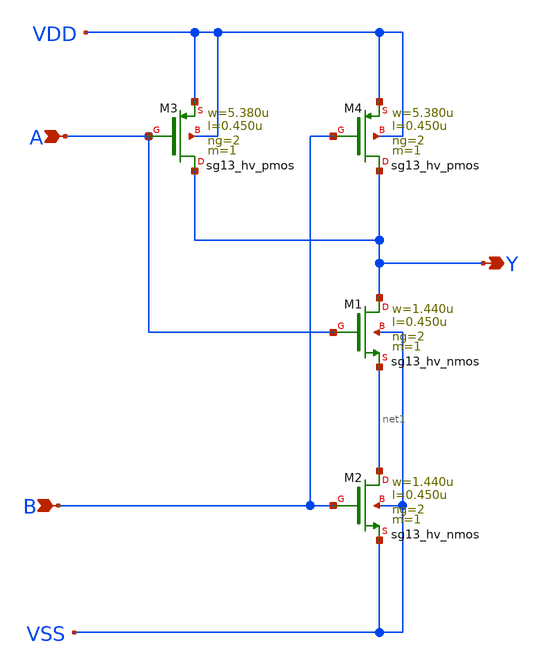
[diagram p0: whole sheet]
** sch_path: ihp-sg13g2/libs.ref/sg13g2_stdcell_hv/sch/xschem/sg13g2_hv_nand2_2.sch
* Copyright 2023 IHP PDK Authors
* Licensed under the Apache License, Version 2.0 (the "License");
* you may not use this file except in compliance with the License.
* You may obtain a copy of the License at
* https://www.apache.org/licenses/LICENSE-2.0
* Unless required by applicable law or agreed to in writing, software
* distributed under the License is distributed on an "AS IS" BASIS,
* WITHOUT WARRANTIES OR CONDITIONS OF ANY KIND, either express or implied.
* See the License for the specific language governing permissions and
* limitations under the License.
**.subckt sg13g2_hv_nand2_2 Y B A
*.opin Y
*.ipin B
*.ipin A
XM1 Y A net1 VSS sg13_hv_nmos w=1.440u l=0.450u ng=2 m=1 mm_ok=1
XM2 net1 B VSS VSS sg13_hv_nmos w=1.440u l=0.450u ng=2 m=1 mm_ok=1
XM3 Y A VDD VDD sg13_hv_pmos w=5.380u l=0.450u ng=2 m=1 mm_ok=1
XM4 Y B VDD VDD sg13_hv_pmos w=5.380u l=0.450u ng=2 m=1 mm_ok=1
**.ends
.end
